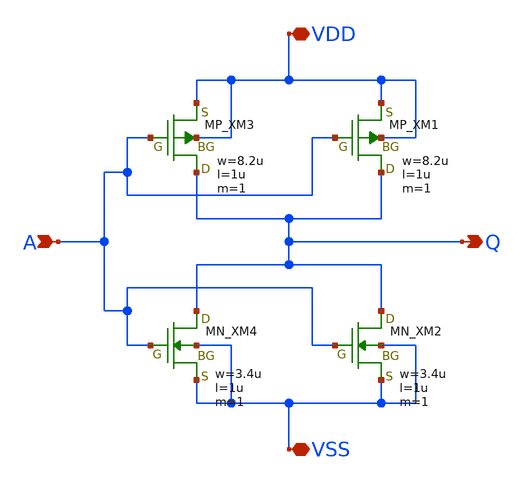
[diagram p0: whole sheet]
** sch_path: member_project/inverter/RISE-A/Talkie_junk/inverter.sch
**.subckt inverter A Q VSS VDD
*.ipin A
*.opin Q
*.iopin VSS
*.iopin VDD
XXM1 Q A VDD VDD PMOS w=8.2u l=1u nrd=0 nrs=0 m=1
XXM2 Q A VSS VSS NMOS w=3.4u l=1u nrd=0 nrs=0 m=1
XXM3 Q A VDD VDD PMOS w=8.2u l=1u nrd=0 nrs=0 m=1
XXM4 Q A VSS VSS NMOS w=3.4u l=1u nrd=0 nrs=0 m=1
**.ends
.end
